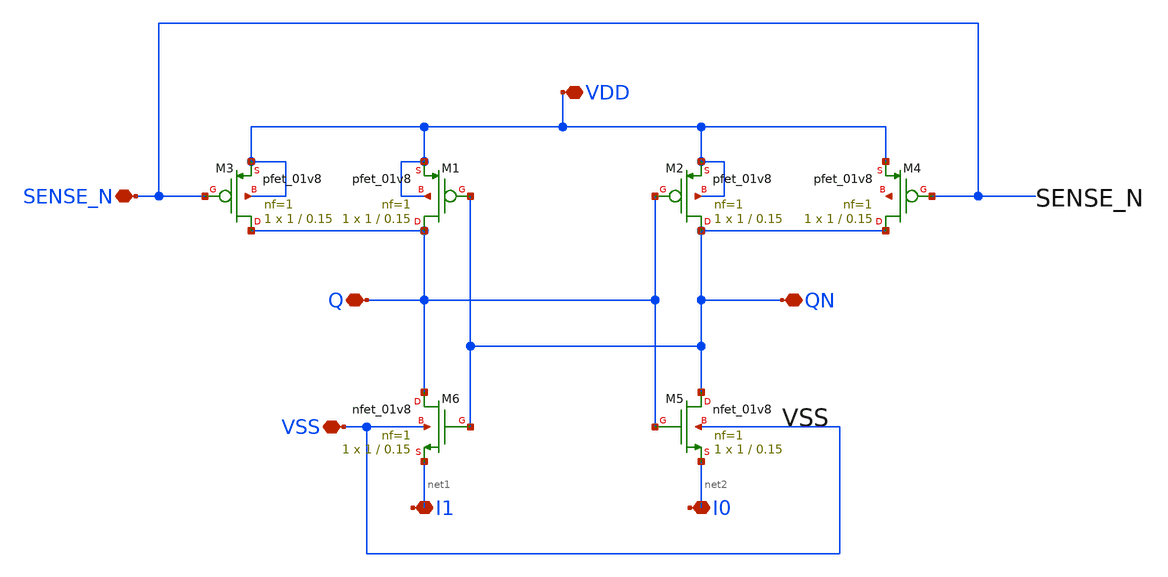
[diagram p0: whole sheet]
** sch_path: SENSEAMP.sch
**.subckt SENSEAMP I1 I0 Q QN SENSE_N VDD VSS
*.iopin I1
*.iopin I0
*.iopin Q
*.iopin QN
*.iopin SENSE_N
*.iopin VDD
*.iopin VSS
XM3 Q SENSE_N VDD VDD sky130_fd_pr__pfet_01v8 L=0.15 W=1 nf=1 ad='int((nf+1)/2) * W/nf * 0.29' as='int((nf+2)/2) * W/nf * 0.29'
+ pd='2*int((nf+1)/2) * (W/nf + 0.29)' ps='2*int((nf+2)/2) * (W/nf + 0.29)' nrd='0.29 / W' nrs='0.29 / W'
+ sa=0 sb=0 sd=0 mult=1 m=1
XM1 Q QN VDD VDD sky130_fd_pr__pfet_01v8 L=0.15 W=1 nf=1 ad='int((nf+1)/2) * W/nf * 0.29' as='int((nf+2)/2) * W/nf * 0.29'
+ pd='2*int((nf+1)/2) * (W/nf + 0.29)' ps='2*int((nf+2)/2) * (W/nf + 0.29)' nrd='0.29 / W' nrs='0.29 / W'
+ sa=0 sb=0 sd=0 mult=1 m=1
XM2 QN Q VDD VDD sky130_fd_pr__pfet_01v8 L=0.15 W=1 nf=1 ad='int((nf+1)/2) * W/nf * 0.29' as='int((nf+2)/2) * W/nf * 0.29'
+ pd='2*int((nf+1)/2) * (W/nf + 0.29)' ps='2*int((nf+2)/2) * (W/nf + 0.29)' nrd='0.29 / W' nrs='0.29 / W'
+ sa=0 sb=0 sd=0 mult=1 m=1
XM4 QN SENSE_N VDD net3 sky130_fd_pr__pfet_01v8 L=0.15 W=1 nf=1 ad='int((nf+1)/2) * W/nf * 0.29' as='int((nf+2)/2) * W/nf * 0.29'
+ pd='2*int((nf+1)/2) * (W/nf + 0.29)' ps='2*int((nf+2)/2) * (W/nf + 0.29)' nrd='0.29 / W' nrs='0.29 / W'
+ sa=0 sb=0 sd=0 mult=1 m=1
XM5 QN Q net2 VSS sky130_fd_pr__nfet_01v8 L=0.15 W=1 nf=1 ad='int((nf+1)/2) * W/nf * 0.29' as='int((nf+2)/2) * W/nf * 0.29'
+ pd='2*int((nf+1)/2) * (W/nf + 0.29)' ps='2*int((nf+2)/2) * (W/nf + 0.29)' nrd='0.29 / W' nrs='0.29 / W'
+ sa=0 sb=0 sd=0 mult=1 m=1
XM6 Q QN net1 VSS sky130_fd_pr__nfet_01v8 L=0.15 W=1 nf=1 ad='int((nf+1)/2) * W/nf * 0.29' as='int((nf+2)/2) * W/nf * 0.29'
+ pd='2*int((nf+1)/2) * (W/nf + 0.29)' ps='2*int((nf+2)/2) * (W/nf + 0.29)' nrd='0.29 / W' nrs='0.29 / W'
+ sa=0 sb=0 sd=0 mult=1 m=1
**** begin user architecture code
I1
**** end user architecture code
**.ends
.end
